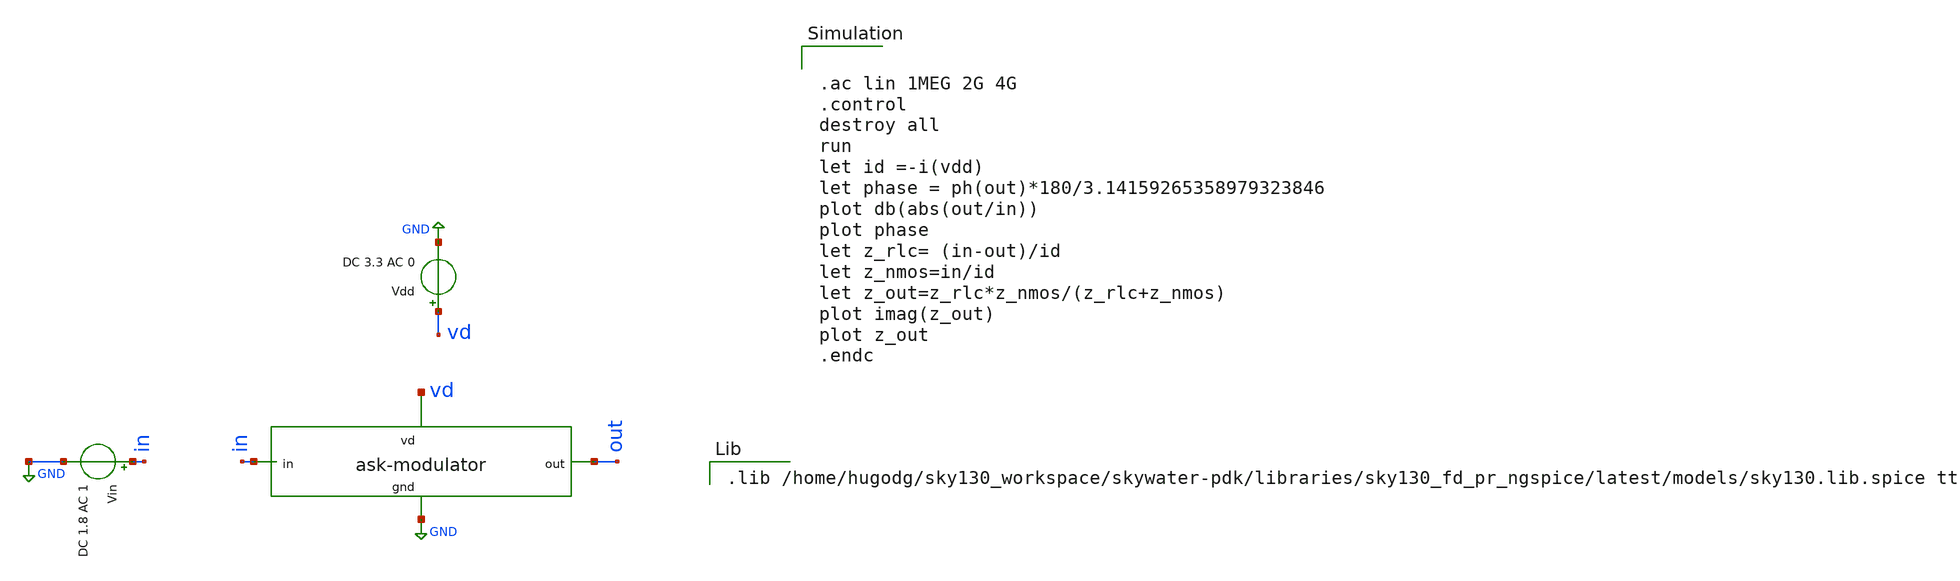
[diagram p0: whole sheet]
** sch_path: ask_modulator/xschem/ask-modulator_tb-ac.sch
**.subckt ask-modulator_tb-ac
Vdd vd GND DC 3.3 AC 0
Vin in GND DC 1.8 AC 1
x1 vd out in GND ask-modulator
**** begin user architecture code


.ac lin 1MEG 2G 4G
.control
destroy all
run
let id =-i(vdd)
let phase = ph(out)*180/3.14159265358979323846
plot db(abs(out/in))
plot phase
let z_rlc= (in-out)/id
let z_nmos=in/id
let z_out=z_rlc*z_nmos/(z_rlc+z_nmos)
plot imag(z_out)
plot z_out
.endc


.lib /home/hugodg/sky130_workspace/skywater-pdk/libraries/sky130_fd_pr_ngspice/latest/models/sky130.lib.spice tt

**** end user architecture code
**.ends
.GLOBAL GND
.end
